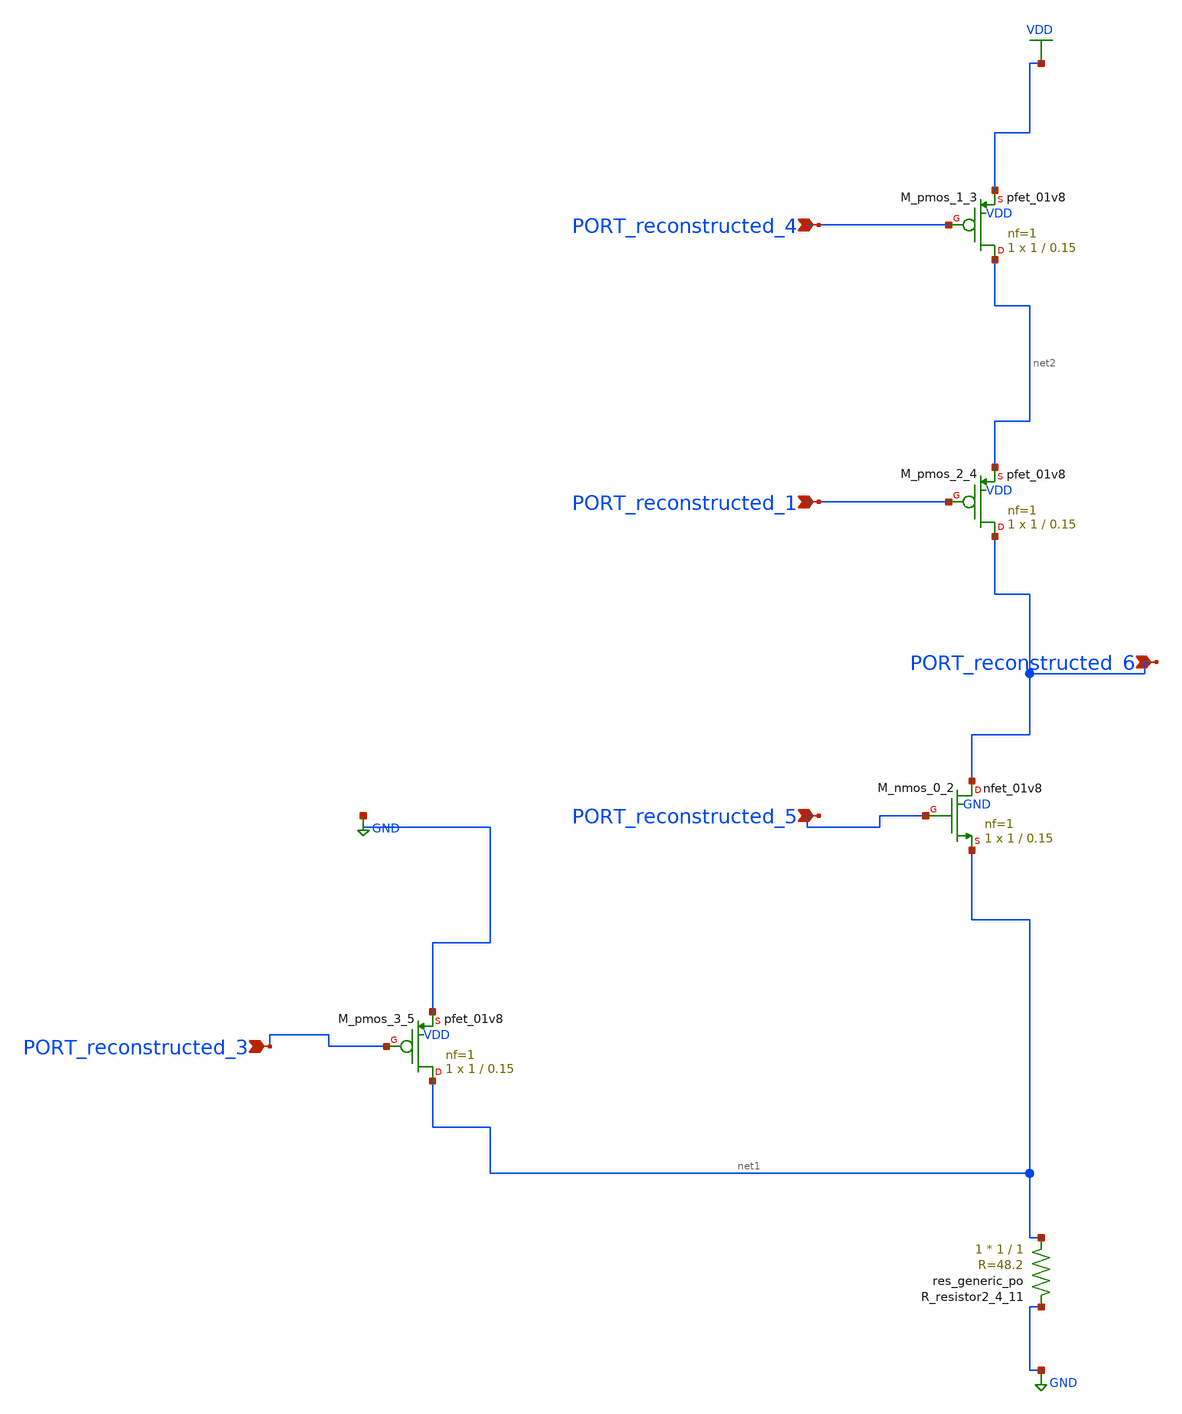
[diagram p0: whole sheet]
** sch_path: schematics/AMSNet/639.sch
**.subckt 639 PORT_reconstructed_1 PORT_reconstructed_4 PORT_reconstructed_5 PORT_reconstructed_3
*+ PORT_reconstructed_6
*.ipin PORT_reconstructed_1
*.ipin PORT_reconstructed_4
*.ipin PORT_reconstructed_5
*.ipin PORT_reconstructed_3
*.ipin PORT_reconstructed_6
XM_nmos_0_2 PORT_reconstructed_6 PORT_reconstructed_5 net1 GND sky130_fd_pr__nfet_01v8 L=0.15 W=1 nf=1
+ ad='int((1 + 1)/2) * 1 / 1 * 0.29' as='int((1 + 2)/2) * 1 / 1 * 0.29' pd='2*int((1 + 1)/2) * (1 / 1 + 0.29)'
+ ps='2*int((1 + 2)/2) * (1 / 1 + 0.29)' nrd='0.29 / 1 ' nrs='0.29 / 1 ' sa=0 sb=0 sd=0 mult=1 m=1
XM_pmos_1_3 net2 PORT_reconstructed_4 VDD VDD sky130_fd_pr__pfet_01v8 L=0.15 W=1 nf=1 ad='int((1 + 1)/2) * 1 / 1 * 0.29'
+ as='int((1 + 2)/2) * 1 / 1 * 0.29' pd='2*int((1 + 1)/2) * (1 / 1 + 0.29)' ps='2*int((1 + 2)/2) * (1 / 1 + 0.29)'
+ nrd='0.29 / 1 ' nrs='0.29 / 1 ' sa=0 sb=0 sd=0 mult=1 m=1
XM_pmos_2_4 PORT_reconstructed_6 PORT_reconstructed_1 net2 VDD sky130_fd_pr__pfet_01v8 L=0.15 W=1 nf=1
+ ad='int((1 + 1)/2) * 1 / 1 * 0.29' as='int((1 + 2)/2) * 1 / 1 * 0.29' pd='2*int((1 + 1)/2) * (1 / 1 + 0.29)'
+ ps='2*int((1 + 2)/2) * (1 / 1 + 0.29)' nrd='0.29 / 1 ' nrs='0.29 / 1 ' sa=0 sb=0 sd=0 mult=1 m=1
XM_pmos_3_5 net1 PORT_reconstructed_3 GND VDD sky130_fd_pr__pfet_01v8 L=0.15 W=1 nf=1 ad='int((1 + 1)/2) * 1 / 1 * 0.29'
+ as='int((1 + 2)/2) * 1 / 1 * 0.29' pd='2*int((1 + 1)/2) * (1 / 1 + 0.29)' ps='2*int((1 + 2)/2) * (1 / 1 + 0.29)'
+ nrd='0.29 / 1 ' nrs='0.29 / 1 ' sa=0 sb=0 sd=0 mult=1 m=1
XR_resistor2_4_11 net1 GND sky130_fd_pr__res_generic_po W=1 L=1 m=1
**.ends
.GLOBAL GND
.GLOBAL VDD
.end
